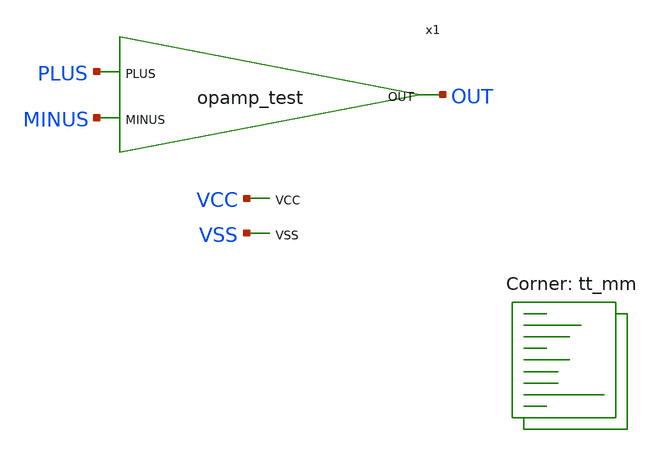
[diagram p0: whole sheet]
** sch_path: xschem/test_bench_opamp.sch
**.subckt test_bench_opamp
x1 OUT PLUS MINUS VCC VSS opamp_test
**** begin user architecture code


.option method=gear

.option wnflag=1

.param VCCGAUSS = agauss(1.8, 0.05, 1)
.param VCC = 'VCCGAUS'

.param TEMPGAUSS = agauss(40, 30, 1)
.option temp = 'TEMPGAUSS'

.include stimuli_test_bench_opamp.cir
.control
	option seed=9
	let run=0
	dowhile run <= 100
		save all
		tran 1n 4000n uic
		remzerovec
		write test_bench_opamp.raw
		set appendwrite
		reset
		let run = run + 1
	end
.endc

.lib $::SKYWATER_MODELS/sky130.lib.spice tt_mm
**** end user architecture code
**.ends

* expanding   symbol:  /home/ttuser/tt_projects/tt10-analog-test-v00/xschem/opamp_test.sym # of
*+ pins=5
** sym_path: xschem/opamp_test.sym
** sch_path: xschem/opamp_test.sch
.subckt opamp_test OUT PLUS MINUS VCC VSS
*.ipin OUT
*.ipin PLUS
*.ipin MINUS
*.ipin VCC
*.ipin VSS
XR1 net3 VCC VSS sky130_fd_pr__res_xhigh_po_2p85 L=2.85 mult=1 m=1
XM1 net2 MINUS net1 VSS sky130_fd_pr__nfet_01v8_lvt L=0.15 W=1 nf=1 ad='int((nf+1)/2) * W/nf * 0.29'
+ as='int((nf+2)/2) * W/nf * 0.29' pd='2*int((nf+1)/2) * (W/nf + 0.29)' ps='2*int((nf+2)/2) * (W/nf + 0.29)'
+ nrd='0.29 / W' nrs='0.29 / W' sa=0 sb=0 sd=0 mult=1 m=1
XM2 net1 net3 VSS VSS sky130_fd_pr__nfet_01v8_lvt L=0.15 W=1 nf=1 ad='int((nf+1)/2) * W/nf * 0.29' as='int((nf+2)/2) * W/nf * 0.29'
+ pd='2*int((nf+1)/2) * (W/nf + 0.29)' ps='2*int((nf+2)/2) * (W/nf + 0.29)' nrd='0.29 / W' nrs='0.29 / W'
+ sa=0 sb=0 sd=0 mult=1 m=1
XM5 net3 net3 VSS VSS sky130_fd_pr__nfet_01v8_lvt L=0.15 W=1 nf=1 ad='int((nf+1)/2) * W/nf * 0.29' as='int((nf+2)/2) * W/nf * 0.29'
+ pd='2*int((nf+1)/2) * (W/nf + 0.29)' ps='2*int((nf+2)/2) * (W/nf + 0.29)' nrd='0.29 / W' nrs='0.29 / W'
+ sa=0 sb=0 sd=0 mult=1 m=1
XM6 OUT PLUS net1 VSS sky130_fd_pr__nfet_01v8_lvt L=0.15 W=1 nf=1 ad='int((nf+1)/2) * W/nf * 0.29' as='int((nf+2)/2) * W/nf * 0.29'
+ pd='2*int((nf+1)/2) * (W/nf + 0.29)' ps='2*int((nf+2)/2) * (W/nf + 0.29)' nrd='0.29 / W' nrs='0.29 / W'
+ sa=0 sb=0 sd=0 mult=1 m=1
XM3 OUT net2 VCC VDD sky130_fd_pr__pfet_01v8_lvt L=0.15 W=1 nf=1 ad='int((nf+1)/2) * W/nf * 0.29' as='int((nf+2)/2) * W/nf * 0.29'
+ pd='2*int((nf+1)/2) * (W/nf + 0.29)' ps='2*int((nf+2)/2) * (W/nf + 0.29)' nrd='0.29 / W' nrs='0.29 / W'
+ sa=0 sb=0 sd=0 mult=1 m=1
XM4 net2 net2 VCC VDD sky130_fd_pr__pfet_01v8_lvt L=0.15 W=1 nf=1 ad='int((nf+1)/2) * W/nf * 0.29' as='int((nf+2)/2) * W/nf * 0.29'
+ pd='2*int((nf+1)/2) * (W/nf + 0.29)' ps='2*int((nf+2)/2) * (W/nf + 0.29)' nrd='0.29 / W' nrs='0.29 / W'
+ sa=0 sb=0 sd=0 mult=1 m=1
.ends

.end
